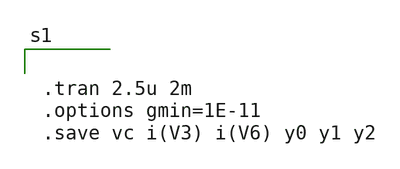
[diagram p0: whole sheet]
** sch_path: xschem/FDC/inverter1_test.sch
**.subckt inverter1_test
**** begin user architecture code

*.lib ~/open_pdks/sky130/sky130A/libs.tech/ngspice/sky130.lib.spice tt
*.MODEL swmod SW(VT=0.0 VH=0.01 RON=1 ROFF=10000000000)
.param mc_mm_switch=0
.param mc_pr_switch=0

.include ~/open_pdks/sky130/sky130A/libs.tech/ngspice/corners/tt/nonfet.spice


*model
.include ~/open_pdks/sky130/sky130A/libs.tech/ngspice/all.spice



*mosfet
.include ~/open_pdks/sky130/sky130A/libs.ref/sky130_fd_pr/spice/sky130_fd_pr__pfet_g5v0d10v5__tt.corner.spice
.inclued ~/open_pdks/sky130/sky130A/libs.ref/sky130_fd_pr/spice/sky130_fd_pr__nfet_g5v0d10v5__tt.corner.spice
*mismatch parameters
.include ~/open_pdks/sky130/sky130A/libs.ref/sky130_fd_pr/spice/sky130_fd_pr__pfet_g5v0d10v5__mismatch.corner.spice
.include ~/open_pdks/sky130/sky130A/libs.ref/sky130_fd_pr/spice/sky130_fd_pr__nfet_g5v0d10v5__mismatch.corner.spice


.tran 2.5u 2m
.options gmin=1E-11
.save vc i(V3) i(V6) y0 y1 y2

**** end user architecture code
**.ends
.end
